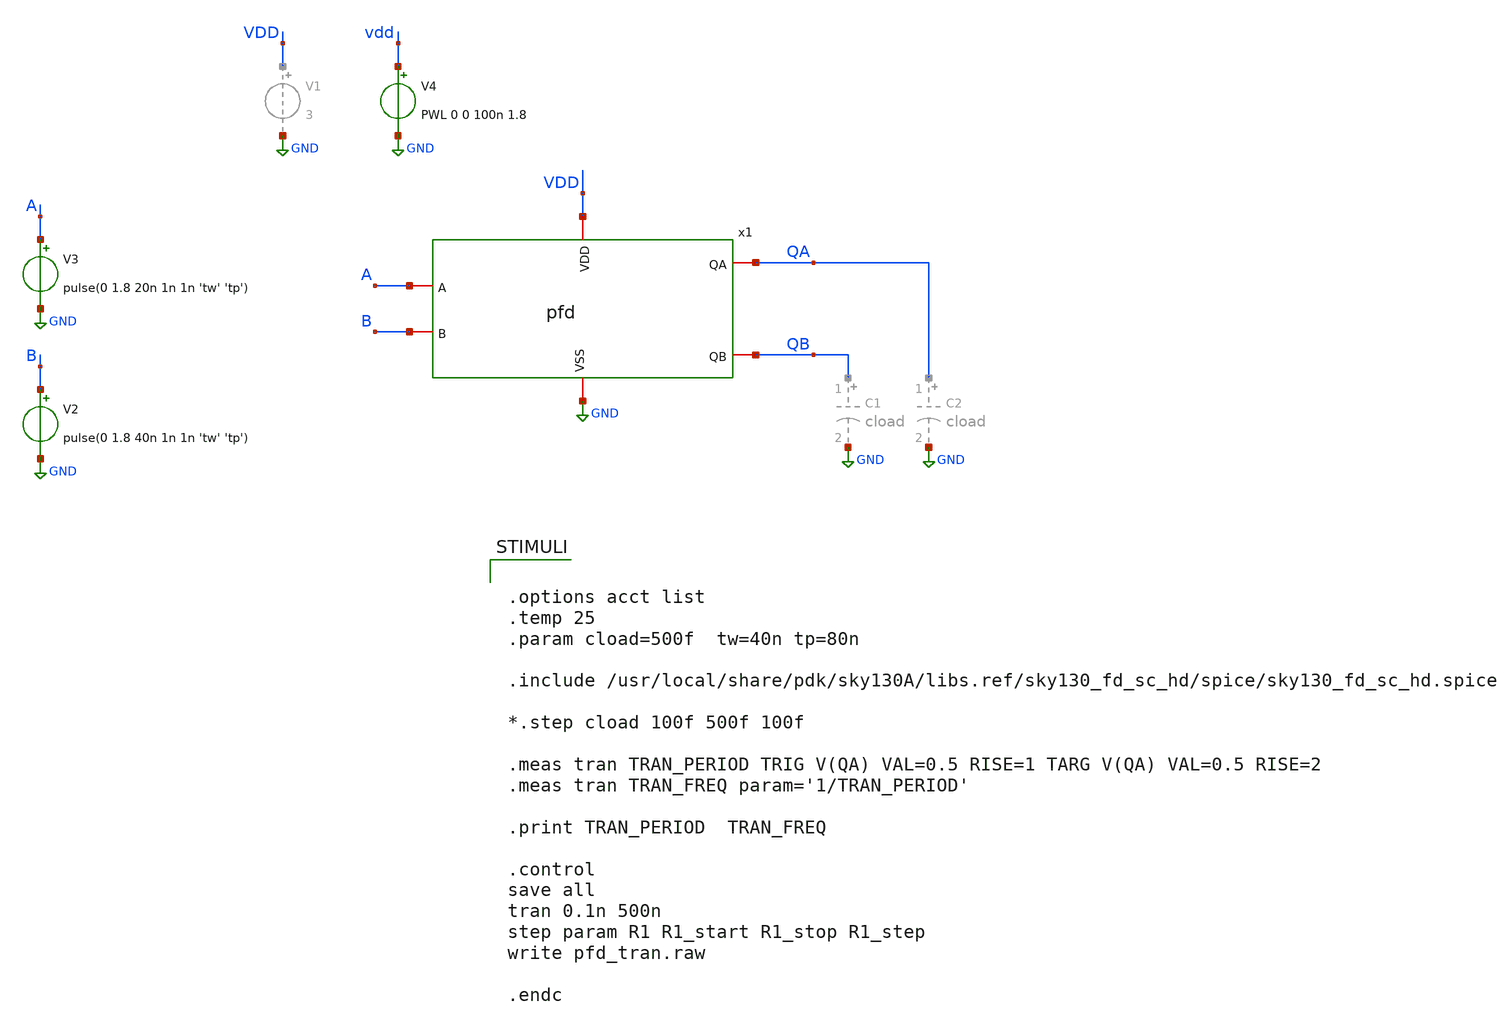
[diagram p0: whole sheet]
** sch_path: xschem01/pfd/pfd_tran.sch
**.subckt pfd_tran
x1 GND VDD A QA QB B pfd
V2 B GND pulse(0 1.8 40n 1n 1n 'tw' 'tp')
V3 A GND pulse(0 1.8 20n 1n 1n 'tw' 'tp')
V4 vdd GND PWL 0 0 100n 1.8
**** begin user architecture code


.options acct list
.temp 25
.param cload=500f  tw=40n tp=80n

.include /usr/local/share/pdk/sky130A/libs.ref/sky130_fd_sc_hd/spice/sky130_fd_sc_hd.spice

*.step cload 100f 500f 100f

.meas tran TRAN_PERIOD TRIG V(QA) VAL=0.5 RISE=1 TARG V(QA) VAL=0.5 RISE=2
.meas tran TRAN_FREQ param='1/TRAN_PERIOD'

.print TRAN_PERIOD  TRAN_FREQ

.control
save all
tran 0.1n 500n
step param R1 R1_start R1_stop R1_step
write pfd_tran.raw

.endc



** opencircuitdesign pdks install
.lib $::SKYWATER_MODELS/sky130.lib.spice tt


**** end user architecture code
**.ends
.GLOBAL GND
.end
